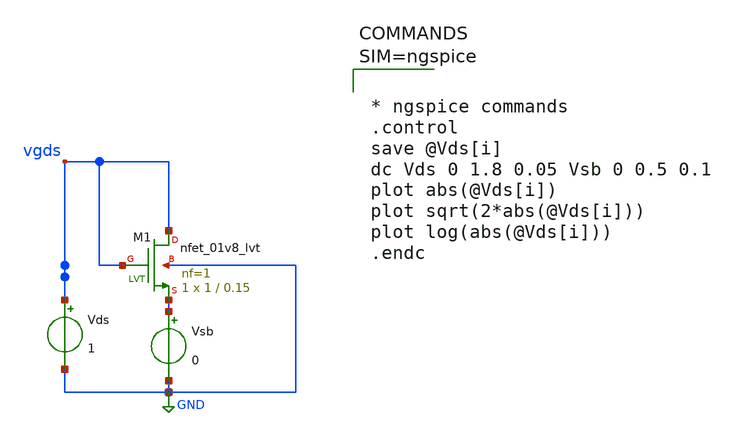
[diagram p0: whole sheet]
** sch_path: xschem/untitled-6.sch
**.subckt untitled-6
XM1 vgds vgds GND GND sky130_fd_pr__nfet_01v8_lvt L=0.15 W=1 nf=1 ad='int((1 + 1)/2) * 1 / 1 * 0.29'
+ as='int((1 + 2)/2) * 1 / 1 * 0.29' pd='2*int((1 + 1)/2) * (1 / 1 + 0.29)' ps='2*int((1 + 2)/2) * (1 / 1 + 0.29)'
+ nrd='0.29 / 1 ' nrs='0.29 / 1 ' sa=0 sb=0 sd=0 mult=1 m=1
Vds vgds GND 1
Vsb GND GND 0
**** begin user architecture code



* ngspice commands
.control
save @Vds[i]
dc Vds 0 1.8 0.05 Vsb 0 0.5 0.1
plot abs(@Vds[i])
plot sqrt(2*abs(@Vds[i]))
plot log(abs(@Vds[i]))
.endc




** opencircuitdesign pdks install
.lib $::SKYWATER_MODELS/sky130.lib.spice tt

**** end user architecture code
**.ends
.GLOBAL GND
.end
